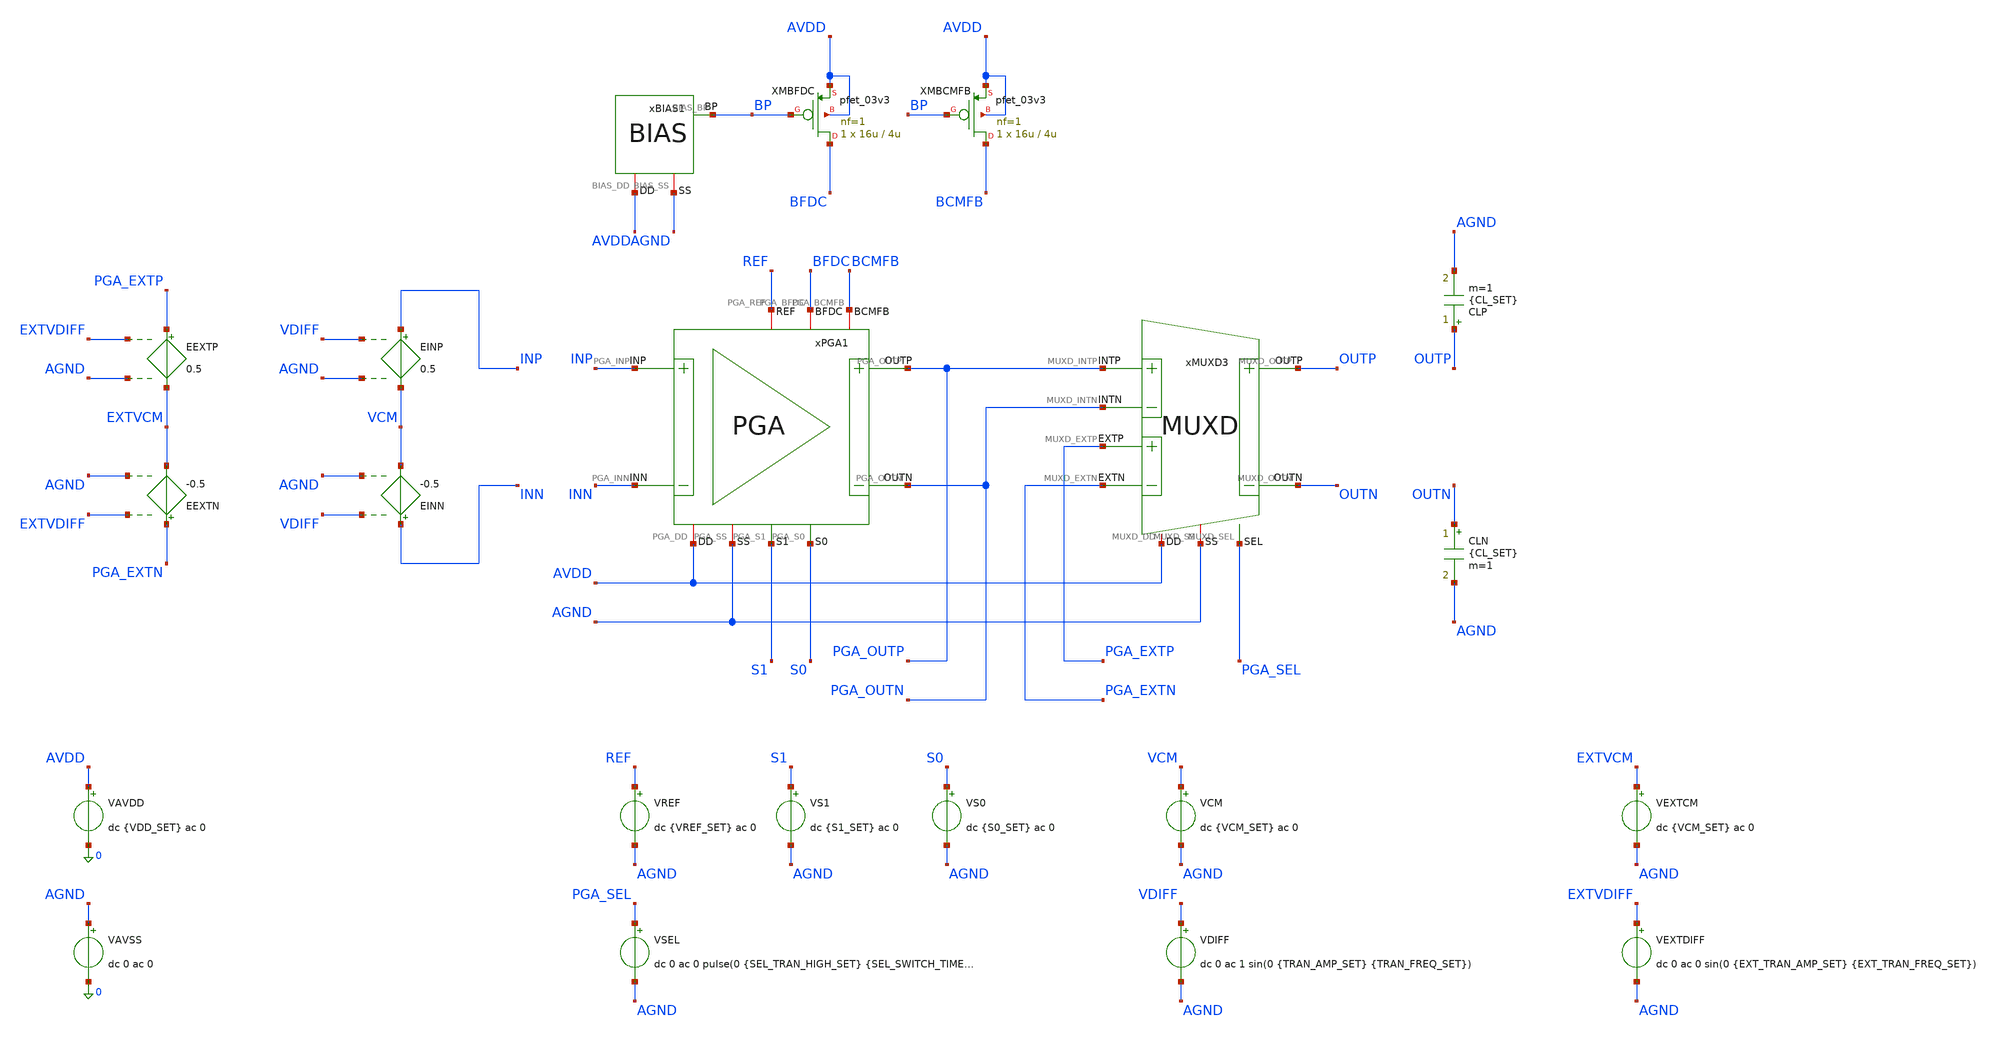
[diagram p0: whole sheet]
** sch_path: Design_Files/IC Design/Testbench/AFE_BLOCKS/PGA/PGA_TB_MC.sch
**.subckt PGA_TB_MC
CLP OUTP AGND {CL_SET} m=1
CLN OUTN AGND {CL_SET} m=1
xBIAS1 AVDD AGND BP BIAS
XMBFDC BFDC BP AVDD AVDD pfet_03v3 L=4u W=16u nf=1 ad='int((nf+1)/2) * W/nf * 0.18u' as='int((nf+2)/2) * W/nf * 0.18u'
+ pd='2*int((nf+1)/2) * (W/nf + 0.18u)' ps='2*int((nf+2)/2) * (W/nf + 0.18u)' nrd='0.18u / W' nrs='0.18u / W'
+ sa=0 sb=0 sd=0 m=1
XMBCMFB BCMFB BP AVDD AVDD pfet_03v3 L=4u W=16u nf=1 ad='int((nf+1)/2) * W/nf * 0.18u' as='int((nf+2)/2) * W/nf * 0.18u'
+ pd='2*int((nf+1)/2) * (W/nf + 0.18u)' ps='2*int((nf+2)/2) * (W/nf + 0.18u)' nrd='0.18u / W' nrs='0.18u / W'
+ sa=0 sb=0 sd=0 m=1
VAVDD AVDD 0 dc {VDD_SET} ac 0
.save i(vavdd)
VAVSS AGND 0 dc 0 ac 0
VCM VCM AGND dc {VCM_SET} ac 0
VDIFF VDIFF AGND dc 0 ac 1 sin(0 {TRAN_AMP_SET} {TRAN_FREQ_SET})
VREF REF AGND dc {VREF_SET} ac 0
VSEL PGA_SEL AGND dc 0 ac 0 pulse(0 {SEL_TRAN_HIGH_SET} {SEL_SWITCH_TIME_SET} 1u 1u 400m 800m)
VEXTCM EXTVCM AGND dc {VCM_SET} ac 0
VEXTDIFF EXTVDIFF AGND dc 0 ac 0 sin(0 {EXT_TRAN_AMP_SET} {EXT_TRAN_FREQ_SET})
EINP INP VCM VDIFF AGND 0.5
EINN INN VCM VDIFF AGND -0.5
EEXTP PGA_EXTP EXTVCM EXTVDIFF AGND 0.5
EEXTN PGA_EXTN EXTVCM EXTVDIFF AGND -0.5
xPGA1 AVDD AGND INP INN PGA_OUTN BFDC PGA_OUTP BCMFB REF S1 S0 PGA
xMUXD3 AVDD AGND PGA_OUTP PGA_OUTN OUTN OUTP PGA_EXTP PGA_EXTN PGA_SEL MUXD
VS1 S1 AGND dc {S1_SET} ac 0
VS0 S0 AGND dc {S0_SET} ac 0
**** begin user architecture code

* {MODELS_START}
.include $::180MCU_MODELS/design.ngspice

.param sw_stat_global=0
.param sw_stat_mismatch=1

.param mc_skew=3
.param res_mc_skew=3
.param cap_mc_skew=3

.lib $::180MCU_MODELS/sm141064.ngspice statistical
.lib $::180MCU_MODELS/sm141064.ngspice res_statistical
.lib $::180MCU_MODELS/sm141064.ngspice mimcap_statistical
.lib $::180MCU_MODELS/sm141064.ngspice cap_mim
.lib $::180MCU_MODELS/sm141064.ngspice bjt_statistical
* {MODELS_END}



* {SETUP_START}
.param VDD_SET=3.3
.param TEMP_SET=27

.param VCM_SET={VDD_SET/2}
.param VREF_SET={VDD_SET/2}

.param CL_SET=10p

.param S1_SET=0
.param S0_SET=0

.param PGA_G2_TARGET_SET=2
.param PGA_G4_TARGET_SET=4
.param PGA_G8_TARGET_SET=8
.param PGA_G16_TARGET_SET=16

.param TRAN_AMP_SET=50m
.param TRAN_FREQ_SET=10

.param EXT_TRAN_AMP_SET=0
.param EXT_TRAN_FREQ_SET=25

.param SEL_TRAN_HIGH_SET=0
.param SEL_SWITCH_TIME_SET=200m

.csparam MC_RUNS=200

.temp {TEMP_SET}

.options gmin=1e-12
.options rshunt=1e12
.options method=gear
* {SETUP_END}




* {MEAS_START}
.control

destroy all

set noaskquit
set wr_singlescale
unset wr_vecnames

option klu
option numdgt=15
option method=gear
option maxord=2
option plotwinsize=0


let mode_index=0

dowhile mode_index < 3

if mode_index = 0
set mode=mm
set tag=mm
alterparam sw_stat_global=0
alterparam sw_stat_mismatch=1
end

if mode_index = 1
set mode=gl
set tag=gl
alterparam sw_stat_global=1
alterparam sw_stat_mismatch=0
end

if mode_index = 2
set mode=full
set tag=full
alterparam sw_stat_global=1
alterparam sw_stat_mismatch=1
end

* Condition

alterparam VDD_SET=3.3
alterparam TEMP_SET=27
alterparam SEL_TRAN_HIGH_SET=0
alterparam EXT_TRAN_AMP_SET=0

reset


* Output

shell mkdir -p /foss/designs/ECG_Acquisition_IC/Measurement_Results/IC_Simulation/AFE_BLOCKS/PGA/{$mode}.Result_txt

shell rm -f /foss/designs/ECG_Acquisition_IC/Measurement_Results/IC_Simulation/AFE_BLOCKS/PGA/{$mode}.Result_txt/{$tag}.op_mc_summary.txt
shell rm -f /foss/designs/ECG_Acquisition_IC/Measurement_Results/IC_Simulation/AFE_BLOCKS/PGA/{$mode}.Result_txt/{$tag}.g2_mc_summary.txt
shell rm -f /foss/designs/ECG_Acquisition_IC/Measurement_Results/IC_Simulation/AFE_BLOCKS/PGA/{$mode}.Result_txt/{$tag}.g4_mc_summary.txt
shell rm -f /foss/designs/ECG_Acquisition_IC/Measurement_Results/IC_Simulation/AFE_BLOCKS/PGA/{$mode}.Result_txt/{$tag}.g8_mc_summary.txt
shell rm -f /foss/designs/ECG_Acquisition_IC/Measurement_Results/IC_Simulation/AFE_BLOCKS/PGA/{$mode}.Result_txt/{$tag}.g16_mc_summary.txt


let run=1

dowhile run <= $&MC_RUNS

setseed $&run
mc_source


* Save after mc_source

save v(AVDD) v(AGND) v(REF)
save v(INP) v(INN)
save v(PGA_OUTP) v(PGA_OUTN)
save i(VAVDD)
save @m.xmbfdc.m0[id]
save @m.xmbcmfb.m0[id]


* Sources

alter @VAVDD[DC]=3.3
alter @VAVSS[DC]=0

alter @VCM[DC]=1.65
alter @VREF[DC]=1.65

alter @VSEL[DC]=0
alter @VDIFF[DC]=0

alter @VAVDD[ACMAG]=0
alter @VAVSS[ACMAG]=0
alter @VCM[ACMAG]=0
alter @VREF[ACMAG]=0
alter @VDIFF[ACMAG]=0
alter @VEXTDIFF[ACMAG]=0


* Four gains

foreach gcode 0 1 2 3

if $gcode = 0
set gtag=g2
set gain_target=2
set s1v=0
set s0v=0
else
if $gcode = 1
set gtag=g4
set gain_target=4
set s1v=0
set s0v=3.3
else
if $gcode = 2
set gtag=g8
set gain_target=8
set s1v=3.3
set s0v=0
else
set gtag=g16
set gain_target=16
set s1v=3.3
set s0v=3.3
end
end
end

alter @VS1[DC]=$s1v
alter @VS0[DC]=$s0v

alter @VDIFF[DC]=0

alter @VDIFF[ACMAG]=0
alter @VCM[ACMAG]=0
alter @VREF[ACMAG]=0
alter @VAVDD[ACMAG]=0
alter @VAVSS[ACMAG]=0
alter @VEXTDIFF[ACMAG]=0


* Offset

dc VDIFF -10m 10m 50u

let pga_diff=v(PGA_OUTP)-v(PGA_OUTN)

meas dc vos_meas when pga_diff=0 cross=1

set vos_val=$&vos_meas

destroy all


* Shared OP at G2

if $gcode = 0

alter @VDIFF[DC]=$vos_val

op

let pga_out_cm=0.5*(v(PGA_OUTP)+v(PGA_OUTN))-v(AGND)
let out_cm_error=pga_out_cm-v(REF)

let idd_total=abs(vavdd#branch)
let power_total=(v(AVDD)-v(AGND))*idd_total

let ibfdc=abs(@m.xmbfdc.m0[id])
let ibcmfb=abs(@m.xmbcmfb.m0[id])

set ibfdc_val=$&ibfdc
set ibcmfb_val=$&ibcmfb
set idd_val=$&idd_total
set power_val=$&power_total
set outcmerr_val=$&out_cm_error

echo $&run $ibfdc_val $ibcmfb_val $idd_val $power_val $outcmerr_val >> /foss/designs/ECG_Acquisition_IC/Measurement_Results/IC_Simulation/AFE_BLOCKS/PGA/{$mode}.Result_txt/{$tag}.op_mc_summary.txt

destroy all

end


* Differential AC

alter @VDIFF[DC]=$vos_val

alter @VDIFF[ACMAG]=1
alter @VCM[ACMAG]=0
alter @VREF[ACMAG]=0
alter @VAVDD[ACMAG]=0
alter @VAVSS[ACMAG]=0
alter @VEXTDIFF[ACMAG]=0

ac dec 50 10 20Meg

let vin_diff=v(INP)-v(INN)
let pga_diff=v(PGA_OUTP)-v(PGA_OUTN)

let pga_gain=mag(pga_diff/vin_diff)

meas ac gain10 find pga_gain at=10
meas ac gain60 find pga_gain at=60
meas ac gain150 find pga_gain at=150

let norm_db=20*log10(pga_gain/$&gain10)

meas ac bw3db when norm_db=-3 fall=1

set gain10_val=$&gain10
set gain60_val=$&gain60
set gain150_val=$&gain150
set bw3db_val=$&bw3db

if $gcode = 0
let gain_error_pct=100*($&gain10/2-1)
else
if $gcode = 1
let gain_error_pct=100*($&gain10/4-1)
else
if $gcode = 2
let gain_error_pct=100*($&gain10/8-1)
else
let gain_error_pct=100*($&gain10/16-1)
end
end
end

set gainerr_val=$&gain_error_pct

destroy all


* CMRR 60 Hz

alter @VDIFF[ACMAG]=0
alter @VCM[ACMAG]=1

ac lin 1 60 60

let vin_cm=v(INP)
let pga_diff=v(PGA_OUTP)-v(PGA_OUTN)

let acm60=mag(pga_diff/vin_cm)

set acm60_val=$&acm60

destroy all


* CMRR 150 Hz

ac lin 1 150 150

let vin_cm=v(INP)
let pga_diff=v(PGA_OUTP)-v(PGA_OUTN)

let acm150=mag(pga_diff/vin_cm)

set acm150_val=$&acm150

let cmrr60=20*log10($gain60_val/$acm60_val)
let cmrr150=20*log10($gain150_val/$acm150_val)

set cmrr60_val=$&cmrr60
set cmrr150_val=$&cmrr150

destroy all


* Gain output

echo $&run $vos_val $gain10_val $gainerr_val $gain150_val $bw3db_val $cmrr60_val $cmrr150_val >> /foss/designs/ECG_Acquisition_IC/Measurement_Results/IC_Simulation/AFE_BLOCKS/PGA/{$mode}.Result_txt/{$tag}.{$gtag}_mc_summary.txt

end


let run=run+1

end

let mode_index=mode_index+1

end

quit

.endc
* {MEAS_END}


**** end user architecture code
**.ends
.end
